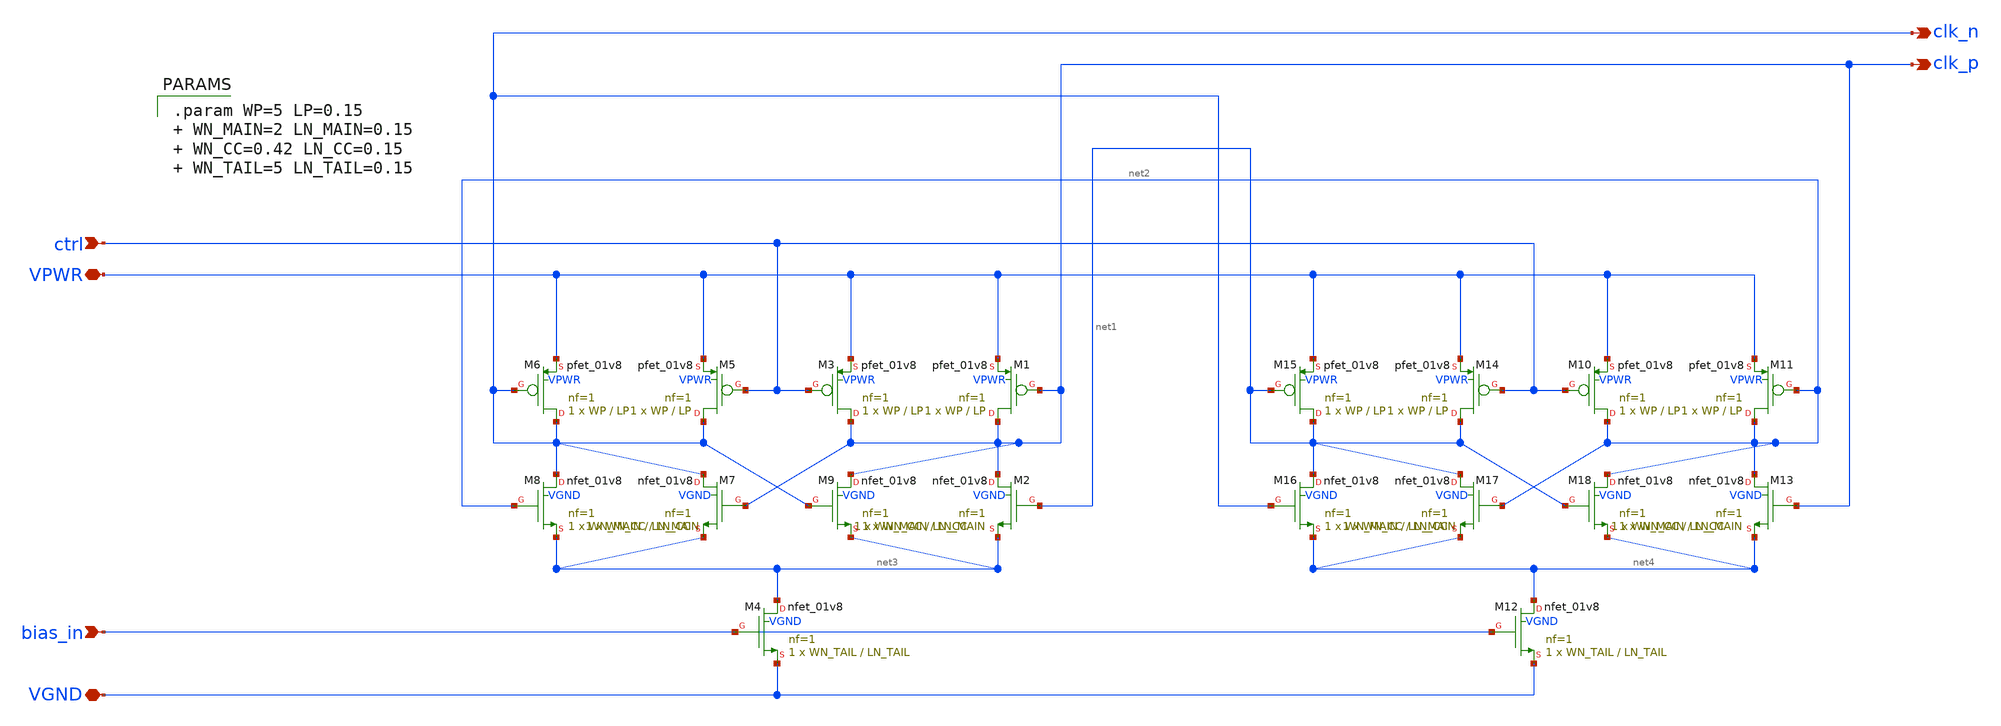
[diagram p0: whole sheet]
** sch_path: simple_vco/v1/clk_core.sch
**.subckt clk_core VPWR VGND ctrl bias_in clk_p clk_n
*.iopin VPWR
*.iopin VGND
*.ipin ctrl
*.ipin bias_in
*.opin clk_p
*.opin clk_n
XM3 clk_p ctrl VPWR VPWR sky130_fd_pr__pfet_01v8 L=LP W=WP nf=1 ad='int((1 + 1)/2) * WP / 1 * 0.29' as='int((1 + 2)/2) * WP / 1 * 0.29'
+ pd='2*int((1 + 1)/2) * (WP / 1 + 0.29)' ps='2*int((1 + 2)/2) * (WP / 1 + 0.29)' nrd='0.29 / WP ' nrs='0.29 / WP '
+ sa=0 sb=0 sd=0 mult=1 m=1
XM1 clk_p clk_p VPWR VPWR sky130_fd_pr__pfet_01v8 L=LP W=WP nf=1 ad='int((1 + 1)/2) * WP / 1 * 0.29'
+ as='int((1 + 2)/2) * WP / 1 * 0.29' pd='2*int((1 + 1)/2) * (WP / 1 + 0.29)' ps='2*int((1 + 2)/2) * (WP / 1 + 0.29)'
+ nrd='0.29 / WP ' nrs='0.29 / WP ' sa=0 sb=0 sd=0 mult=1 m=1
XM4 net3 bias_in VGND VGND sky130_fd_pr__nfet_01v8 L=LN_TAIL W=WN_TAIL nf=1 ad='int((1 + 1)/2) * WN_TAIL / 1 * 0.29'
+ as='int((1 + 2)/2) * WN_TAIL / 1 * 0.29' pd='2*int((1 + 1)/2) * (WN_TAIL / 1 + 0.29)' ps='2*int((1 + 2)/2) * (WN_TAIL / 1 + 0.29)'
+ nrd='0.29 / WN_TAIL ' nrs='0.29 / WN_TAIL ' sa=0 sb=0 sd=0 mult=1 m=1
XM2 clk_p net1 net3 VGND sky130_fd_pr__nfet_01v8 L=LN_MAIN W=WN_MAIN nf=1 ad='int((1 + 1)/2) * WN_MAIN / 1 * 0.29'
+ as='int((1 + 2)/2) * WN_MAIN / 1 * 0.29' pd='2*int((1 + 1)/2) * (WN_MAIN / 1 + 0.29)' ps='2*int((1 + 2)/2) * (WN_MAIN / 1 + 0.29)'
+ nrd='0.29 / WN_MAIN ' nrs='0.29 / WN_MAIN ' sa=0 sb=0 sd=0 mult=1 m=1
XM5 clk_n ctrl VPWR VPWR sky130_fd_pr__pfet_01v8 L=LP W=WP nf=1 ad='int((1 + 1)/2) * WP / 1 * 0.29' as='int((1 + 2)/2) * WP / 1 * 0.29'
+ pd='2*int((1 + 1)/2) * (WP / 1 + 0.29)' ps='2*int((1 + 2)/2) * (WP / 1 + 0.29)' nrd='0.29 / WP ' nrs='0.29 / WP '
+ sa=0 sb=0 sd=0 mult=1 m=1
XM6 clk_n clk_n VPWR VPWR sky130_fd_pr__pfet_01v8 L=LP W=WP nf=1 ad='int((1 + 1)/2) * WP / 1 * 0.29'
+ as='int((1 + 2)/2) * WP / 1 * 0.29' pd='2*int((1 + 1)/2) * (WP / 1 + 0.29)' ps='2*int((1 + 2)/2) * (WP / 1 + 0.29)'
+ nrd='0.29 / WP ' nrs='0.29 / WP ' sa=0 sb=0 sd=0 mult=1 m=1
XM8 clk_n net2 net3 VGND sky130_fd_pr__nfet_01v8 L=LN_MAIN W=WN_MAIN nf=1 ad='int((1 + 1)/2) * WN_MAIN / 1 * 0.29'
+ as='int((1 + 2)/2) * WN_MAIN / 1 * 0.29' pd='2*int((1 + 1)/2) * (WN_MAIN / 1 + 0.29)' ps='2*int((1 + 2)/2) * (WN_MAIN / 1 + 0.29)'
+ nrd='0.29 / WN_MAIN ' nrs='0.29 / WN_MAIN ' sa=0 sb=0 sd=0 mult=1 m=1
XM7 clk_n clk_p net3 VGND sky130_fd_pr__nfet_01v8 L=LN_CC W=WN_CC nf=1 ad='int((1 + 1)/2) * WN_CC / 1 * 0.29'
+ as='int((1 + 2)/2) * WN_CC / 1 * 0.29' pd='2*int((1 + 1)/2) * (WN_CC / 1 + 0.29)' ps='2*int((1 + 2)/2) * (WN_CC / 1 + 0.29)'
+ nrd='0.29 / WN_CC ' nrs='0.29 / WN_CC ' sa=0 sb=0 sd=0 mult=1 m=1
XM9 clk_p clk_n net3 VGND sky130_fd_pr__nfet_01v8 L=LN_CC W=WN_CC nf=1 ad='int((1 + 1)/2) * WN_CC / 1 * 0.29'
+ as='int((1 + 2)/2) * WN_CC / 1 * 0.29' pd='2*int((1 + 1)/2) * (WN_CC / 1 + 0.29)' ps='2*int((1 + 2)/2) * (WN_CC / 1 + 0.29)'
+ nrd='0.29 / WN_CC ' nrs='0.29 / WN_CC ' sa=0 sb=0 sd=0 mult=1 m=1
XM10 net2 ctrl VPWR VPWR sky130_fd_pr__pfet_01v8 L=LP W=WP nf=1 ad='int((1 + 1)/2) * WP / 1 * 0.29' as='int((1 + 2)/2) * WP / 1 * 0.29'
+ pd='2*int((1 + 1)/2) * (WP / 1 + 0.29)' ps='2*int((1 + 2)/2) * (WP / 1 + 0.29)' nrd='0.29 / WP ' nrs='0.29 / WP '
+ sa=0 sb=0 sd=0 mult=1 m=1
XM11 net2 net2 VPWR VPWR sky130_fd_pr__pfet_01v8 L=LP W=WP nf=1 ad='int((1 + 1)/2) * WP / 1 * 0.29' as='int((1 + 2)/2) * WP / 1 * 0.29'
+ pd='2*int((1 + 1)/2) * (WP / 1 + 0.29)' ps='2*int((1 + 2)/2) * (WP / 1 + 0.29)' nrd='0.29 / WP ' nrs='0.29 / WP '
+ sa=0 sb=0 sd=0 mult=1 m=1
XM12 net4 bias_in VGND VGND sky130_fd_pr__nfet_01v8 L=LN_TAIL W=WN_TAIL nf=1 ad='int((1 + 1)/2) * WN_TAIL / 1 * 0.29'
+ as='int((1 + 2)/2) * WN_TAIL / 1 * 0.29' pd='2*int((1 + 1)/2) * (WN_TAIL / 1 + 0.29)' ps='2*int((1 + 2)/2) * (WN_TAIL / 1 + 0.29)'
+ nrd='0.29 / WN_TAIL ' nrs='0.29 / WN_TAIL ' sa=0 sb=0 sd=0 mult=1 m=1
XM13 net2 clk_p net4 VGND sky130_fd_pr__nfet_01v8 L=LN_MAIN W=WN_MAIN nf=1 ad='int((1 + 1)/2) * WN_MAIN / 1 * 0.29'
+ as='int((1 + 2)/2) * WN_MAIN / 1 * 0.29' pd='2*int((1 + 1)/2) * (WN_MAIN / 1 + 0.29)' ps='2*int((1 + 2)/2) * (WN_MAIN / 1 + 0.29)'
+ nrd='0.29 / WN_MAIN ' nrs='0.29 / WN_MAIN ' sa=0 sb=0 sd=0 mult=1 m=1
XM14 net1 ctrl VPWR VPWR sky130_fd_pr__pfet_01v8 L=LP W=WP nf=1 ad='int((1 + 1)/2) * WP / 1 * 0.29' as='int((1 + 2)/2) * WP / 1 * 0.29'
+ pd='2*int((1 + 1)/2) * (WP / 1 + 0.29)' ps='2*int((1 + 2)/2) * (WP / 1 + 0.29)' nrd='0.29 / WP ' nrs='0.29 / WP '
+ sa=0 sb=0 sd=0 mult=1 m=1
XM15 net1 net1 VPWR VPWR sky130_fd_pr__pfet_01v8 L=LP W=WP nf=1 ad='int((1 + 1)/2) * WP / 1 * 0.29' as='int((1 + 2)/2) * WP / 1 * 0.29'
+ pd='2*int((1 + 1)/2) * (WP / 1 + 0.29)' ps='2*int((1 + 2)/2) * (WP / 1 + 0.29)' nrd='0.29 / WP ' nrs='0.29 / WP '
+ sa=0 sb=0 sd=0 mult=1 m=1
XM16 net1 clk_n net4 VGND sky130_fd_pr__nfet_01v8 L=LN_MAIN W=WN_MAIN nf=1 ad='int((1 + 1)/2) * WN_MAIN / 1 * 0.29'
+ as='int((1 + 2)/2) * WN_MAIN / 1 * 0.29' pd='2*int((1 + 1)/2) * (WN_MAIN / 1 + 0.29)' ps='2*int((1 + 2)/2) * (WN_MAIN / 1 + 0.29)'
+ nrd='0.29 / WN_MAIN ' nrs='0.29 / WN_MAIN ' sa=0 sb=0 sd=0 mult=1 m=1
XM17 net1 net2 net4 VGND sky130_fd_pr__nfet_01v8 L=LN_CC W=WN_CC nf=1 ad='int((1 + 1)/2) * WN_CC / 1 * 0.29'
+ as='int((1 + 2)/2) * WN_CC / 1 * 0.29' pd='2*int((1 + 1)/2) * (WN_CC / 1 + 0.29)' ps='2*int((1 + 2)/2) * (WN_CC / 1 + 0.29)'
+ nrd='0.29 / WN_CC ' nrs='0.29 / WN_CC ' sa=0 sb=0 sd=0 mult=1 m=1
XM18 net2 net1 net4 VGND sky130_fd_pr__nfet_01v8 L=LN_CC W=WN_CC nf=1 ad='int((1 + 1)/2) * WN_CC / 1 * 0.29'
+ as='int((1 + 2)/2) * WN_CC / 1 * 0.29' pd='2*int((1 + 1)/2) * (WN_CC / 1 + 0.29)' ps='2*int((1 + 2)/2) * (WN_CC / 1 + 0.29)'
+ nrd='0.29 / WN_CC ' nrs='0.29 / WN_CC ' sa=0 sb=0 sd=0 mult=1 m=1
**** begin user architecture code

.param WP=5 LP=0.15  WN_MAIN=2 LN_MAIN=0.15  WN_CC=0.42 LN_CC=0.15  WN_TAIL=5 LN_TAIL=0.15


**** end user architecture code
**.ends
.end
